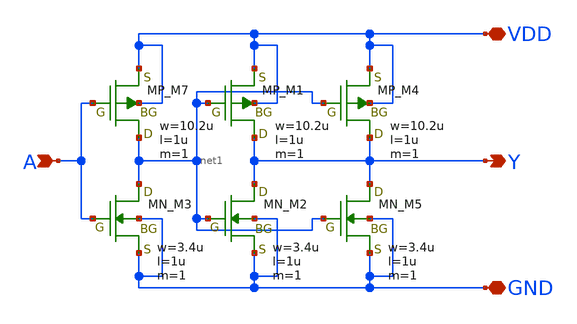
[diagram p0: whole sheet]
** sch_path: lef/BUF_X2.sch
**.subckt BUF_X2 A Y VDD GND
*.ipin A
*.opin Y
*.iopin VDD
*.iopin GND
XM7 net1 A VDD VDD PMOS w=10.2u l=1u as=0 ad=0 ps=0 pd=0 nrd=0 nrs=0 m=1
XM1 Y net1 VDD VDD PMOS w=10.2u l=1u as=0 ad=0 ps=0 pd=0 nrd=0 nrs=0 m=1
XM3 net1 A GND GND NMOS w=3.4u l=1u as=0 ad=0 ps=0 pd=0 nrd=0 nrs=0 m=1
XM2 Y net1 GND GND NMOS w=3.4u l=1u as=0 ad=0 ps=0 pd=0 nrd=0 nrs=0 m=1
XM4 Y net1 VDD VDD PMOS w=10.2u l=1u as=0 ad=0 ps=0 pd=0 nrd=0 nrs=0 m=1
XM5 Y net1 GND GND NMOS w=3.4u l=1u as=0 ad=0 ps=0 pd=0 nrd=0 nrs=0 m=1
**.ends
.end
